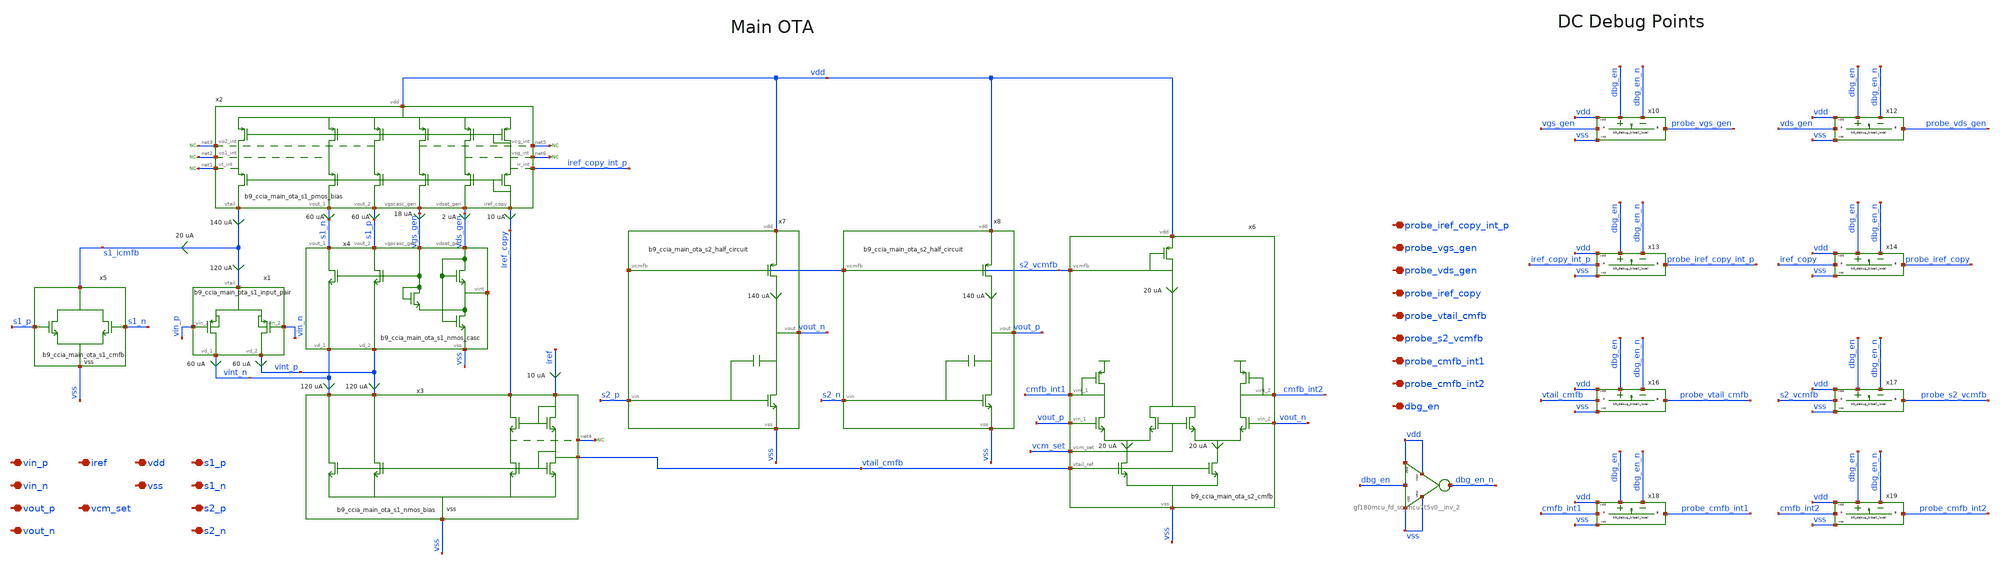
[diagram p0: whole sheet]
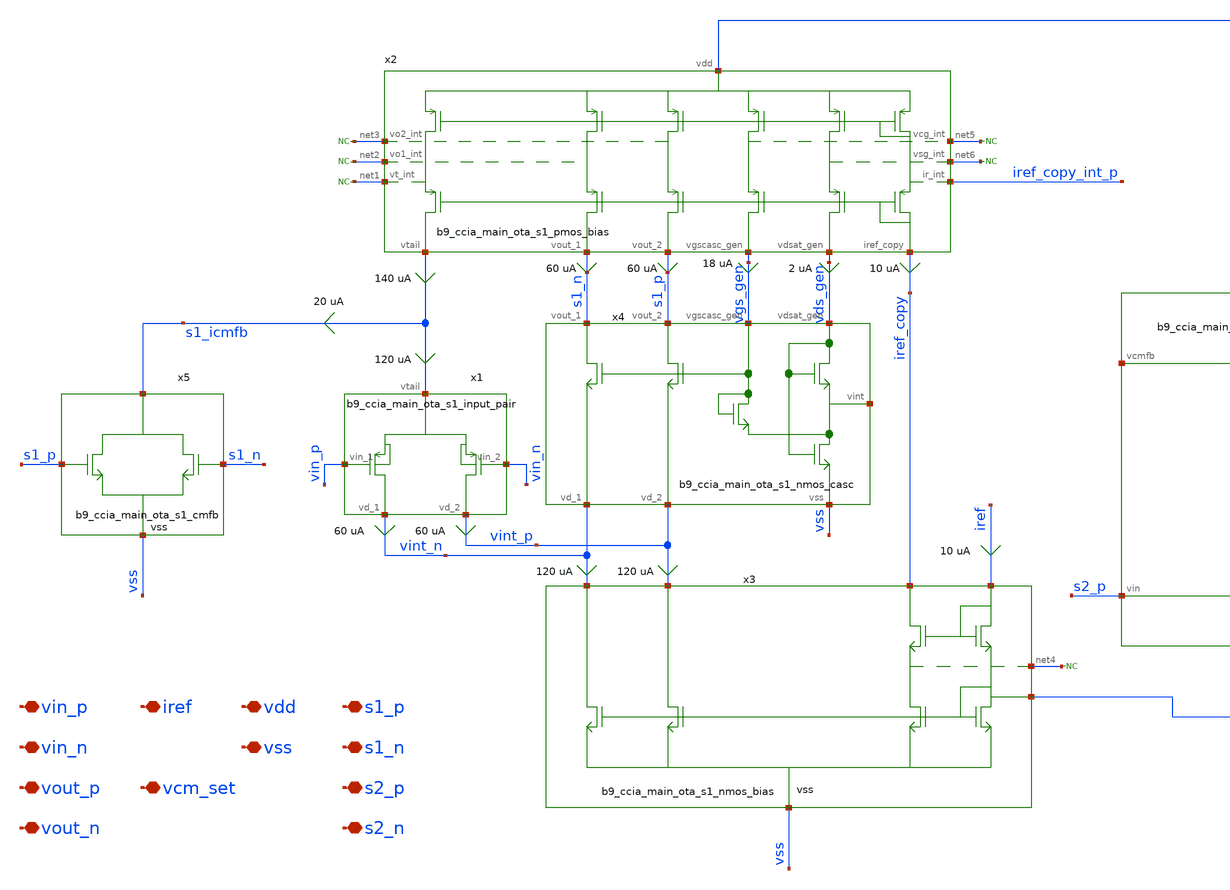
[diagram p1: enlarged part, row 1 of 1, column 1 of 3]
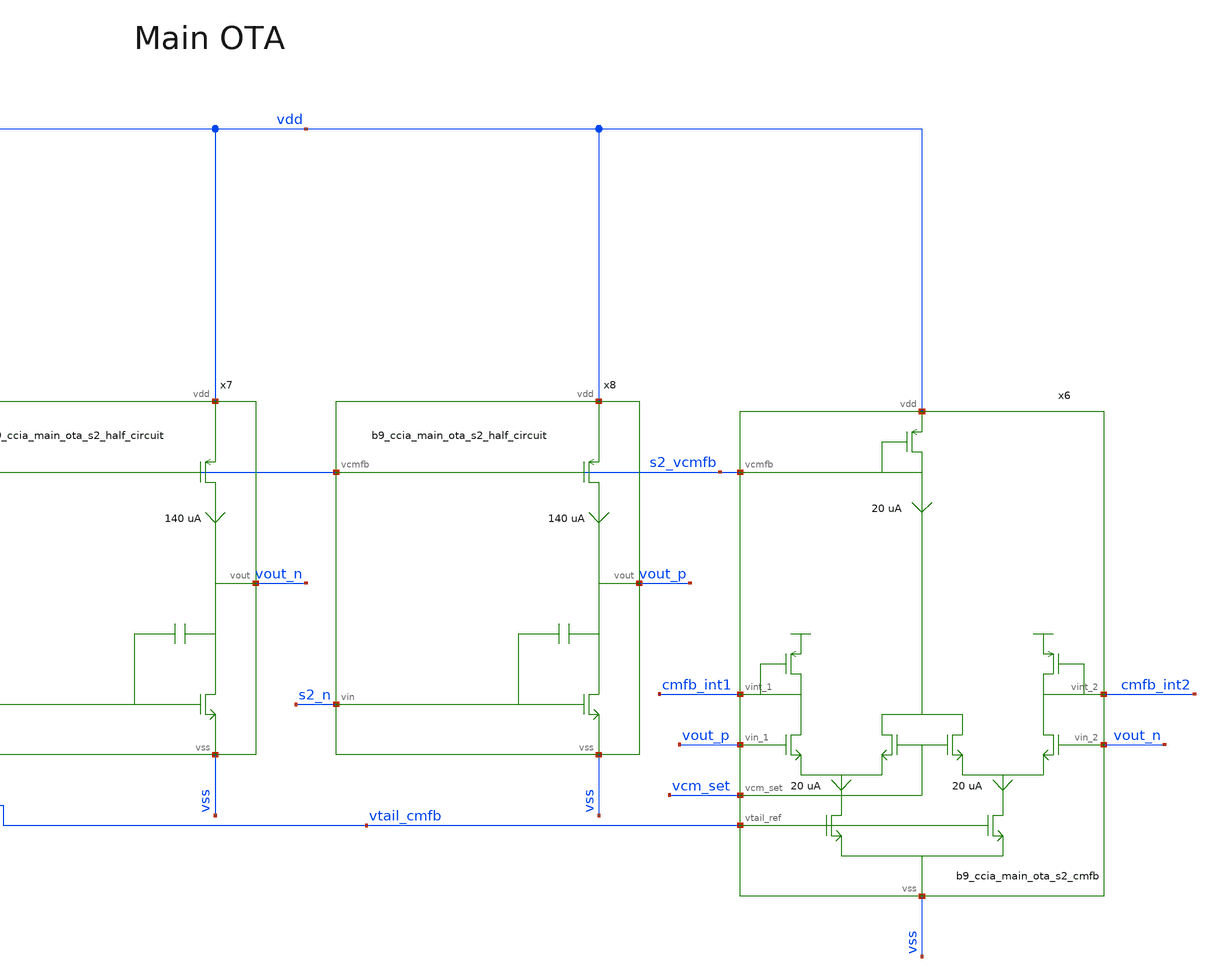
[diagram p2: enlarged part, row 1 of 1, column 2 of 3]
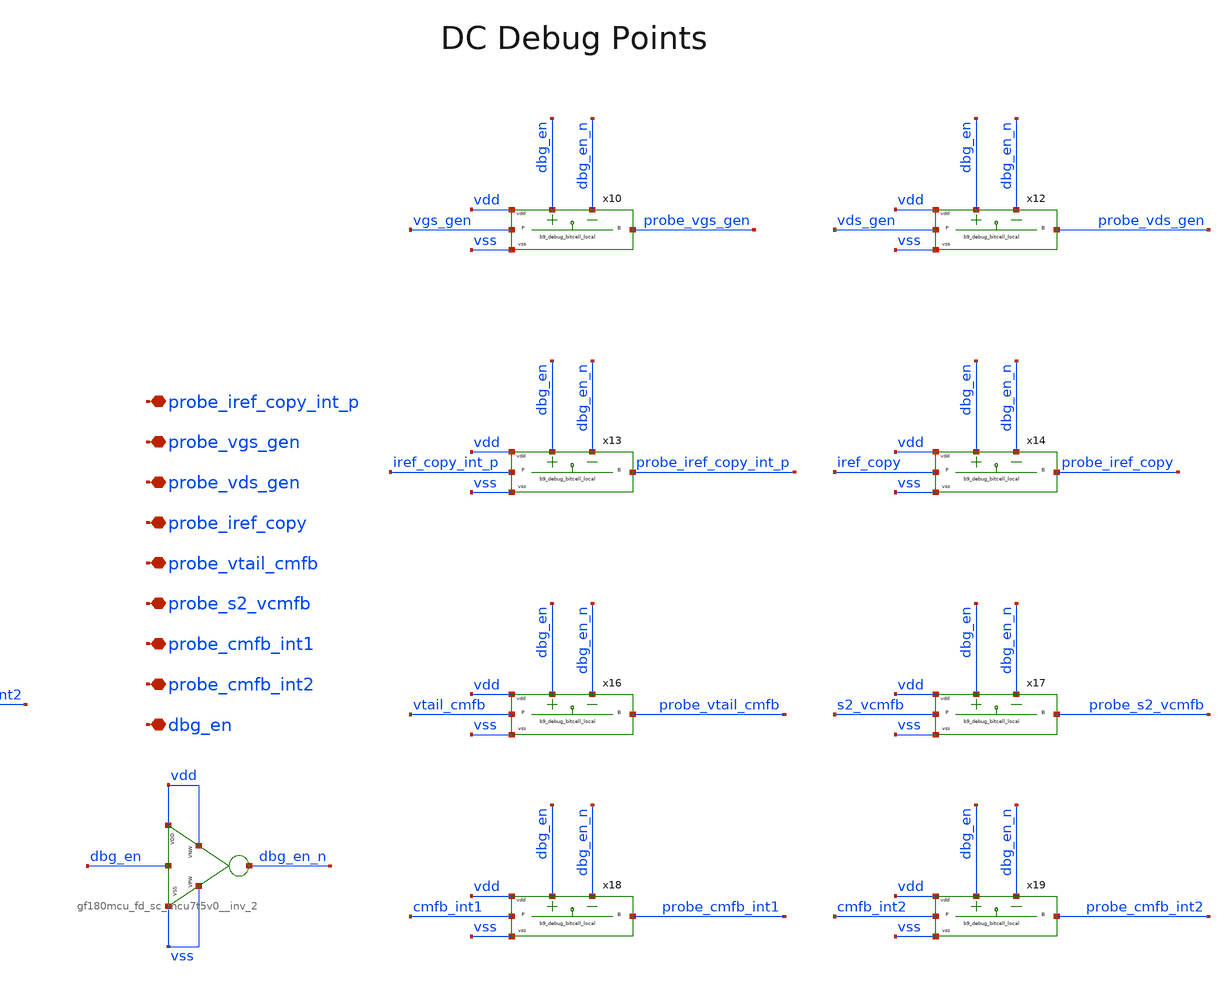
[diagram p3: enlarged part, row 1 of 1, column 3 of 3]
** sch_path: xschem/ccia_main_ota/b9_ccia_main_ota.sch
**.subckt b9_ccia_main_ota probe_iref_copy_int_p probe_vgs_gen probe_vds_gen probe_iref_copy dbg_en
*+ probe_vtail_cmfb probe_s2_vcmfb probe_cmfb_int1 probe_cmfb_int2 vin_p vin_n vout_p vout_n iref vdd vss vcm_set s1_p
*+ s1_n s2_p s2_n
*.iopin probe_iref_copy_int_p
*.iopin probe_vgs_gen
*.iopin probe_vds_gen
*.iopin probe_iref_copy
*.iopin dbg_en
*.iopin probe_vtail_cmfb
*.iopin probe_s2_vcmfb
*.iopin probe_cmfb_int1
*.iopin probe_cmfb_int2
*.iopin vin_p
*.iopin vin_n
*.iopin vout_p
*.iopin vout_n
*.iopin iref
*.iopin vdd
*.iopin vss
*.iopin vcm_set
*.iopin s1_p
*.iopin s1_n
*.iopin s2_p
*.iopin s2_n
x10 dbg_en dbg_en_n vgs_gen probe_vgs_gen vdd vss b9_debug_bitcell_local
x12 dbg_en dbg_en_n vds_gen probe_vds_gen vdd vss b9_debug_bitcell_local
x15 dbg_en dbg_en_n vdd vdd vss vss gf180mcu_fd_sc_mcu7t5v0__inv_2
x13 dbg_en dbg_en_n iref_copy_int_p probe_iref_copy_int_p vdd vss b9_debug_bitcell_local
x14 dbg_en dbg_en_n iref_copy probe_iref_copy vdd vss b9_debug_bitcell_local
x16 dbg_en dbg_en_n vtail_cmfb probe_vtail_cmfb vdd vss b9_debug_bitcell_local
x17 dbg_en dbg_en_n s2_vcmfb probe_s2_vcmfb vdd vss b9_debug_bitcell_local
x18 dbg_en dbg_en_n cmfb_int1 probe_cmfb_int1 vdd vss b9_debug_bitcell_local
x19 dbg_en dbg_en_n cmfb_int2 probe_cmfb_int2 vdd vss b9_debug_bitcell_local
x2 vdd s1_icmfb s1_n s1_p vgs_gen vds_gen iref_copy net1 net2 net3 net5 net6 iref_copy_int_p
+ b9_ccia_main_ota_s1_pmos_bias
x5 s1_icmfb s1_p s1_n vss b9_ccia_main_ota_s1_cmfb
x1 vint_n vint_p vin_p vin_n s1_icmfb b9_ccia_main_ota_s1_input_pair
x4 s1_n s1_p vint_n vint_p vgs_gen vds_gen vss net7 b9_ccia_main_ota_s1_nmos_casc
x3 iref iref_copy vint_n vint_p vss vtail_cmfb net4 b9_ccia_main_ota_s1_nmos_bias
x7 s2_vcmfb vdd vss s2_p vout_n b9_ccia_main_ota_s2_half_circuit
x8 s2_vcmfb vdd vss s2_n vout_p b9_ccia_main_ota_s2_half_circuit
x6 vout_p vout_n vcm_set vtail_cmfb s2_vcmfb vdd vss cmfb_int1 cmfb_int2 b9_ccia_main_ota_s2_cmfb
* noconn #net3
* noconn #net2
* noconn #net1
* noconn #net4
* noconn #net5
* noconn #net6
**.ends
.end
